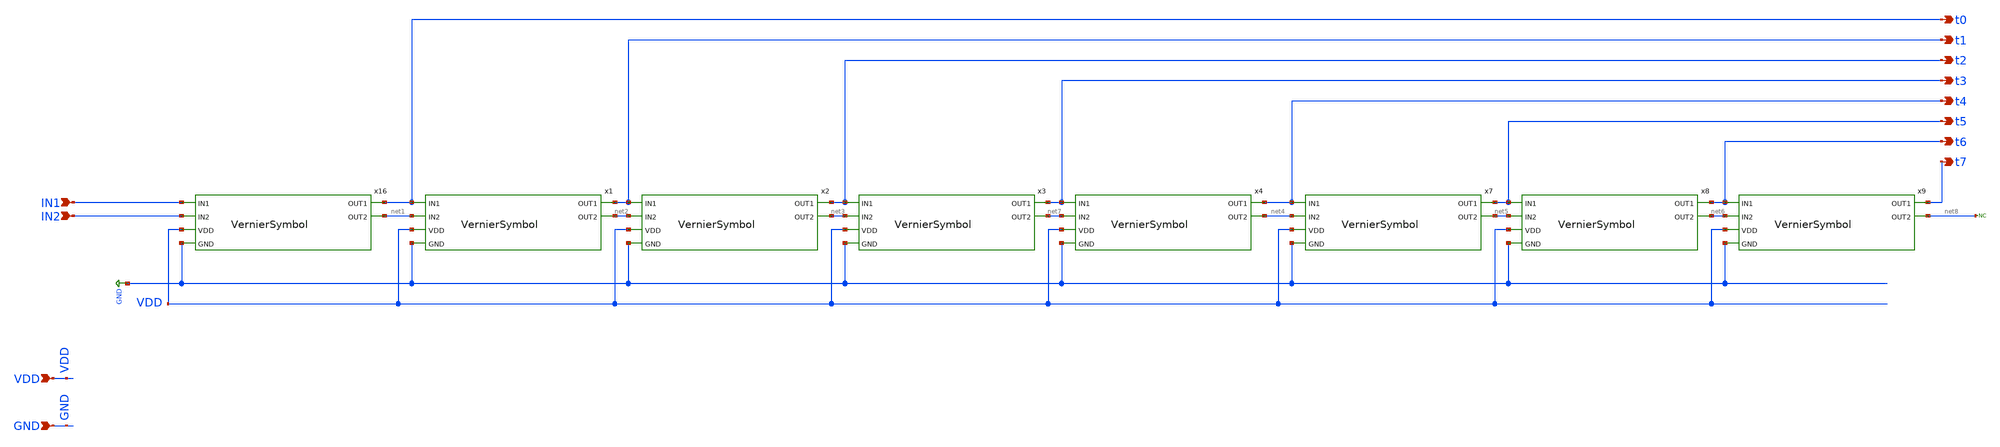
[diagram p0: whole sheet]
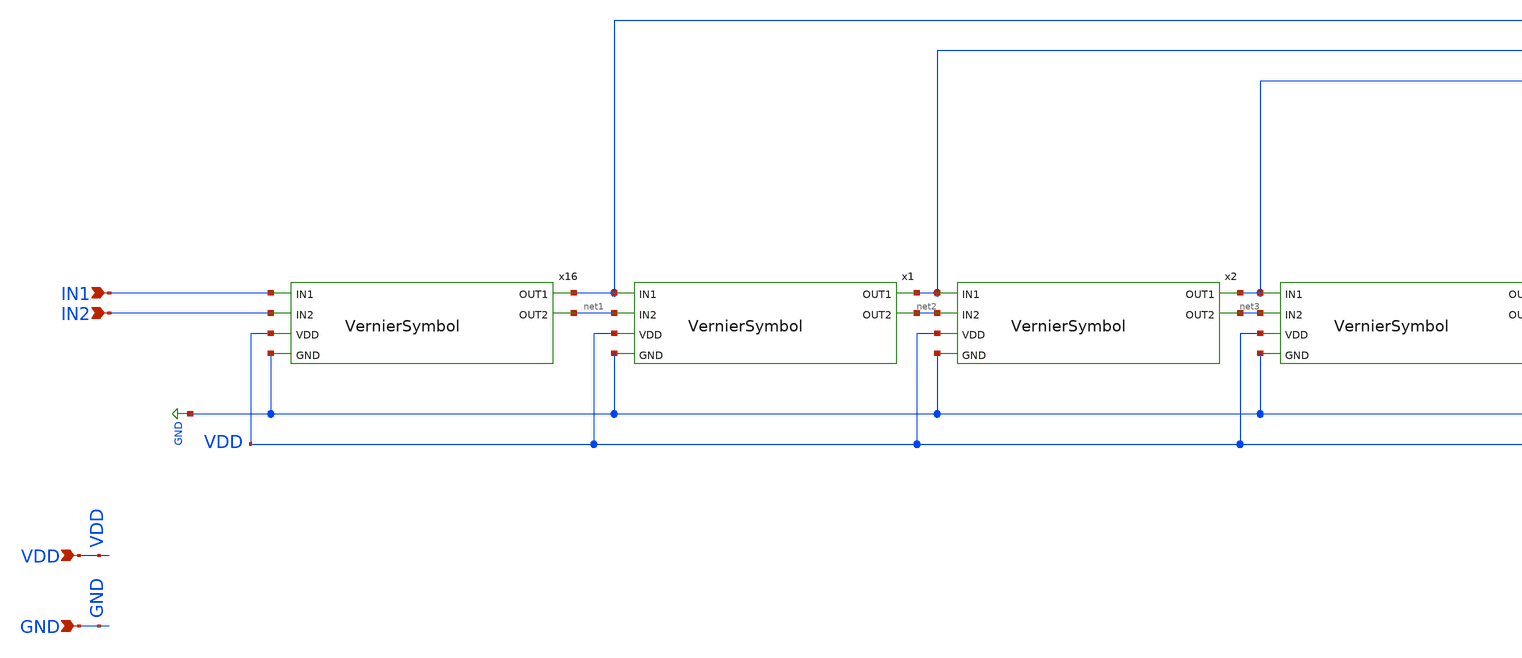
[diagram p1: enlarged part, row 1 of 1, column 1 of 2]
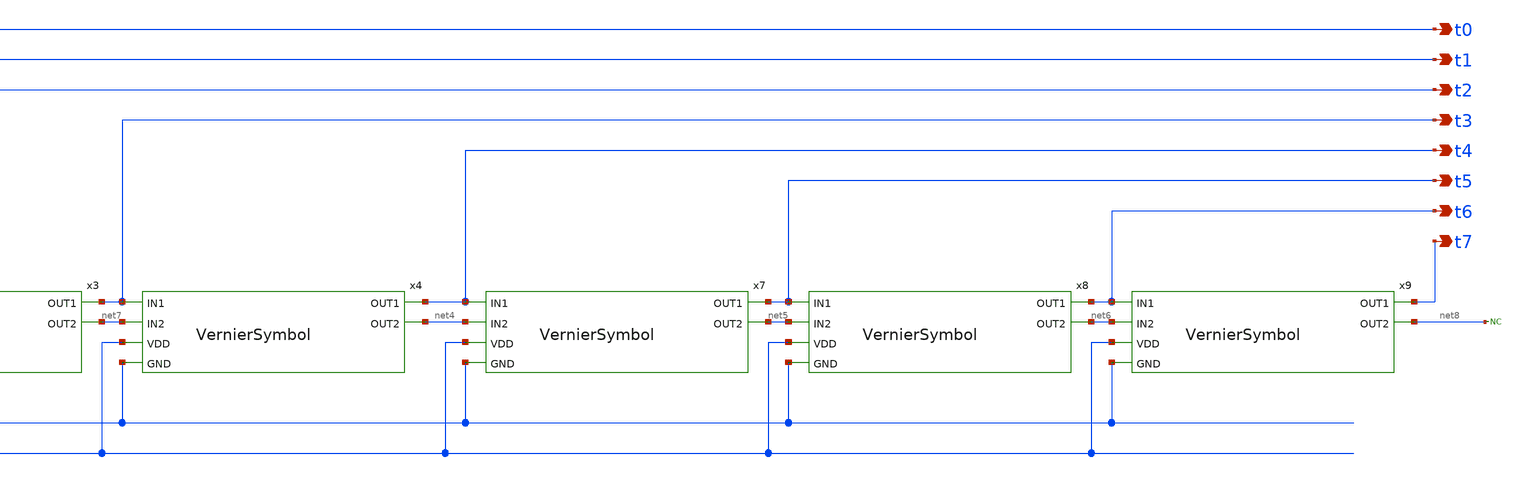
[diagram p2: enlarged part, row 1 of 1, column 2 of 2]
** sch_path: xschem/projects/Vernier8Bit.sch
**.subckt Vernier8Bit VDD GND IN1 IN2 t0 t7 t1 t2 t3 t4 t5 t6
*.ipin VDD
*.ipin GND
*.ipin IN1
*.ipin IN2
*.opin t0
*.opin t7
*.opin t1
*.opin t2
*.opin t3
*.opin t4
*.opin t5
*.opin t6
x16 t0 IN1 net1 IN2 VDD GND VernierSymbol
x1 t1 t0 net2 net1 VDD GND VernierSymbol
x2 t2 t1 net3 net2 VDD GND VernierSymbol
x3 t3 t2 net7 net3 VDD GND VernierSymbol
x4 t4 t3 net4 net7 VDD GND VernierSymbol
x7 t5 t4 net5 net4 VDD GND VernierSymbol
x8 t6 t5 net6 net5 VDD GND VernierSymbol
x9 t7 t6 net8 net6 VDD GND VernierSymbol
* noconn #net8
**.ends

* expanding   symbol:  VernierSymbol.sym # of pins=6
** sym_path: xschem/projects/VernierSymbol.sym
** sch_path: xschem/projects/VernierSymbol.sch
.subckt VernierSymbol OUT1 IN1 OUT2 IN2 VDD GND
*.ipin VDD
*.ipin GND
*.ipin IN1
*.ipin IN2
*.opin OUT1
*.opin OUT2
x2 net8 OUT2 0 0 VDD VDD OUT1 sky130_fd_sc_hd__dlxtp_1
x10 net5 GND GND VDD VDD net7 sky130_fd_sc_hd__buf_1
x11 net4 GND GND VDD VDD net5 sky130_fd_sc_hd__buf_1
x12 IN2 GND GND VDD VDD net4 sky130_fd_sc_hd__buf_1
x6 net3 GND GND VDD VDD net6 sky130_fd_sc_hd__buf_1
x7 net2 GND GND VDD VDD net3 sky130_fd_sc_hd__buf_1
x8 net1 GND GND VDD VDD net2 sky130_fd_sc_hd__buf_1
x9 IN1 GND GND VDD VDD net1 sky130_fd_sc_hd__buf_1
x5 net6 GND GND VDD VDD net8 sky130_fd_sc_hd__buf_1
x13 net7 GND GND VDD VDD OUT2 sky130_fd_sc_hd__buf_1
.ends

.GLOBAL GND
.end
